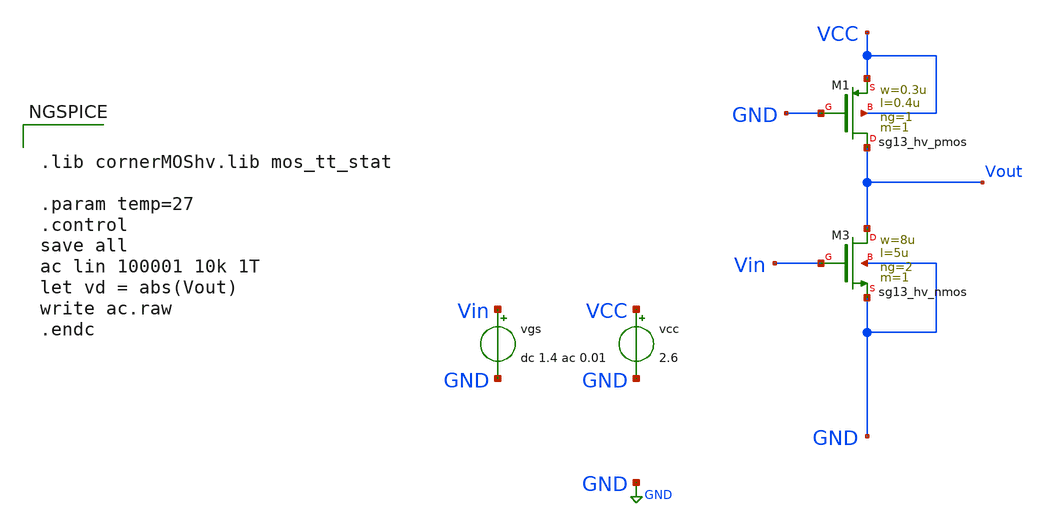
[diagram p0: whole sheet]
** sch_path: lectures/2025-08-28/ac.sch
**.subckt ac
vcc VCC GND 2.6
XM3 Vout Vin GND GND sg13_hv_nmos w=8u l=5u ng=2 m=1 mm_ok=1
XM1 Vout GND VCC VCC sg13_hv_pmos w=0.3u l=0.4u ng=1 m=1 mm_ok=1
vgs Vin GND dc 1.4 ac 0.01
**** begin user architecture code


.lib cornerMOShv.lib mos_tt_stat

.param temp=27
.control
save all
ac lin 100001 10k 1T
let vd = abs(Vout)
write ac.raw
.endc


**** end user architecture code
**.ends
.GLOBAL GND
.end
